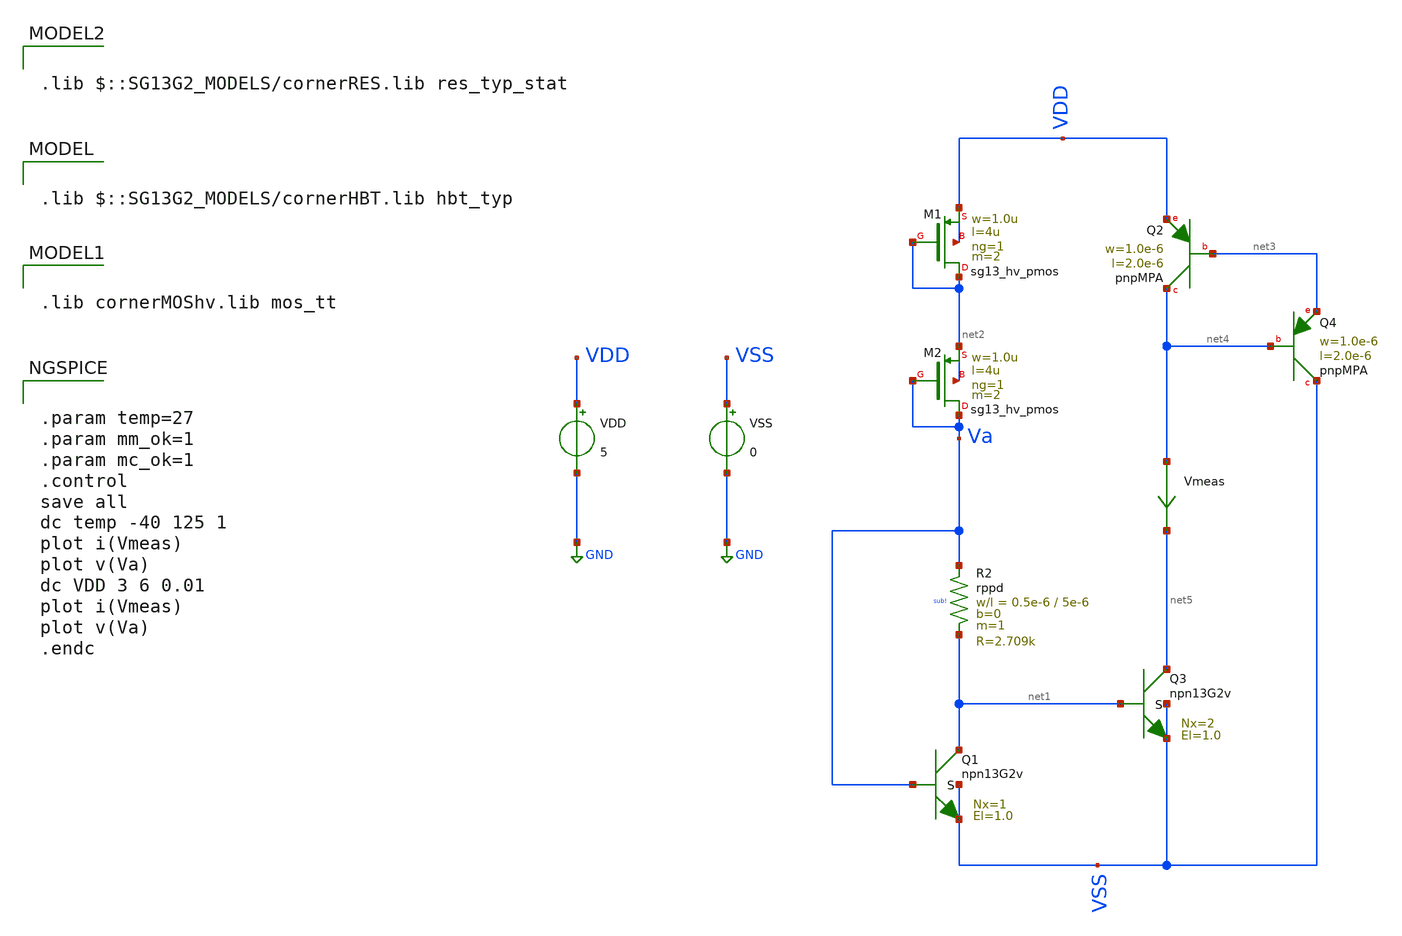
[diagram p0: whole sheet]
** sch_path: Learning/single_ended_amplifiers/A_High_Precision_Micropower_Operational_Amplifier_IHP130_3_3/current_reference/testbench.sch
**.subckt testbench
VDD VDD GND 5
VSS VSS GND 0
XR2 Va net1 sub! rppd w=0.5e-6 l=5e-6 m=1 b=0 mm_ok=1
XQ1 net1 Va VSS VSS npn13G2v Nx=1 El=1.0 mm_ok=1
Vmeas net4 net5 0
.save i(vmeas)
XM1 net2 net2 VDD VDD sg13_hv_pmos w=1.0u l=4u ng=1 m=2 mm_ok=1
XM2 Va Va net2 net2 sg13_hv_pmos w=1.0u l=4u ng=1 m=2 mm_ok=1
XQ2 net4 net3 VDD pnpMPA a=2p p=6u m=1
XQ3 net5 net1 VSS VSS npn13G2v Nx=2 El=1.0 mm_ok=1
XQ4 VSS net4 net3 pnpMPA a=2p p=6u m=1
**** begin user architecture code

.lib $::SG13G2_MODELS/cornerHBT.lib hbt_typ


.lib cornerMOShv.lib mos_tt


.lib $::SG13G2_MODELS/cornerRES.lib res_typ_stat



.param temp=27
.param mm_ok=1
.param mc_ok=1
.control
save all
dc temp -40 125 1
plot i(Vmeas)
plot v(Va)
dc VDD 3 6 0.01
plot i(Vmeas)
plot v(Va)
.endc


**** end user architecture code
**.ends
.GLOBAL GND
.end
